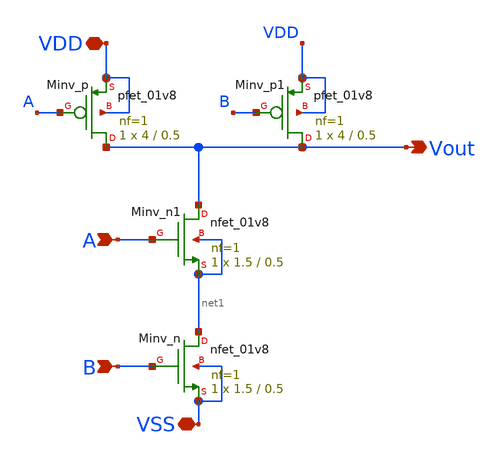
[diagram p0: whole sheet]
** sch_path: xschem/ip_block/logic_gate/nand.sch
**.subckt nand B Vout VDD VSS A
*.ipin B
*.opin Vout
*.iopin VDD
*.iopin VSS
*.ipin A
XMinv_n net1 B VSS VSS sky130_fd_pr__nfet_01v8 L=0.5 W=1.5 nf=1 ad='int((nf+1)/2) * W/nf * 0.29' as='int((nf+2)/2) * W/nf * 0.29'
+ pd='2*int((nf+1)/2) * (W/nf + 0.29)' ps='2*int((nf+2)/2) * (W/nf + 0.29)' nrd='0.29 / W' nrs='0.29 / W'
+ sa=0 sb=0 sd=0 mult=1 m=1
XMinv_p Vout A VDD VDD sky130_fd_pr__pfet_01v8 L=0.5 W=4 nf=1 ad='int((nf+1)/2) * W/nf * 0.29' as='int((nf+2)/2) * W/nf * 0.29'
+ pd='2*int((nf+1)/2) * (W/nf + 0.29)' ps='2*int((nf+2)/2) * (W/nf + 0.29)' nrd='0.29 / W' nrs='0.29 / W'
+ sa=0 sb=0 sd=0 mult=1 m=1
XMinv_n1 Vout A net1 net1 sky130_fd_pr__nfet_01v8 L=0.5 W=1.5 nf=1 ad='int((nf+1)/2) * W/nf * 0.29' as='int((nf+2)/2) * W/nf * 0.29'
+ pd='2*int((nf+1)/2) * (W/nf + 0.29)' ps='2*int((nf+2)/2) * (W/nf + 0.29)' nrd='0.29 / W' nrs='0.29 / W'
+ sa=0 sb=0 sd=0 mult=1 m=1
XMinv_p1 Vout B VDD VDD sky130_fd_pr__pfet_01v8 L=0.5 W=4 nf=1 ad='int((nf+1)/2) * W/nf * 0.29' as='int((nf+2)/2) * W/nf * 0.29'
+ pd='2*int((nf+1)/2) * (W/nf + 0.29)' ps='2*int((nf+2)/2) * (W/nf + 0.29)' nrd='0.29 / W' nrs='0.29 / W'
+ sa=0 sb=0 sd=0 mult=1 m=1
**.ends
.end
